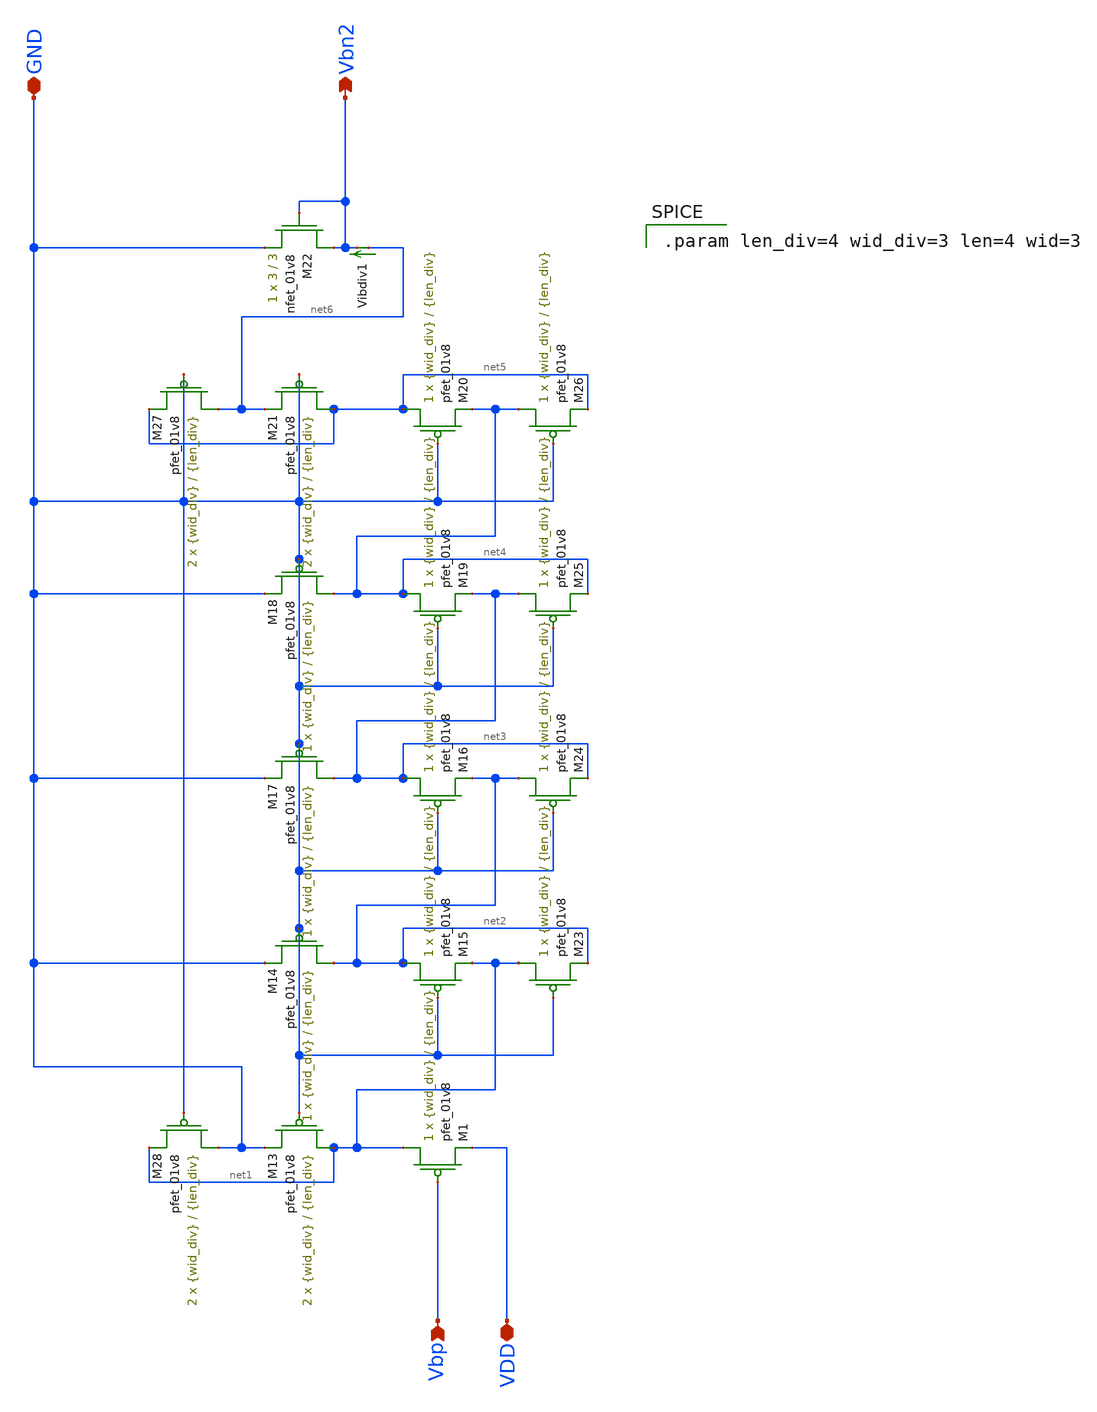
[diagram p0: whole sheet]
** sch_path: mp3/Layout_Schem_Designs/current_divider_lds.sch
**.subckt current_divider_lds GND Vbn2 Vbp VDD
*.iopin GND
*.opin Vbn2
*.ipin Vbp
*.iopin VDD
XM1 net1 Vbp VDD VDD sky130_fd_pr__pfet_01v8 L={len_div} W={wid_div} nf=1 ad='int((nf+1)/2) * W/nf * 0.29'
+ as='int((nf+2)/2) * W/nf * 0.29' pd='2*int((nf+1)/2) * (W/nf + 0.29)' ps='2*int((nf+2)/2) * (W/nf + 0.29)'
+ nrd='0.29 / W' nrs='0.29 / W' sa=0 sb=0 sd=0 mult=1 m=1
XM13 net1 GND GND VDD sky130_fd_pr__pfet_01v8 L={len_div} W={wid_div} nf=1 ad='int((nf+1)/2) * W/nf * 0.29'
+ as='int((nf+2)/2) * W/nf * 0.29' pd='2*int((nf+1)/2) * (W/nf + 0.29)' ps='2*int((nf+2)/2) * (W/nf + 0.29)'
+ nrd='0.29 / W' nrs='0.29 / W' sa=0 sb=0 sd=0 mult=2 m=2
XM14 net2 GND GND VDD sky130_fd_pr__pfet_01v8 L={len_div} W={wid_div} nf=1 ad='int((nf+1)/2) * W/nf * 0.29'
+ as='int((nf+2)/2) * W/nf * 0.29' pd='2*int((nf+1)/2) * (W/nf + 0.29)' ps='2*int((nf+2)/2) * (W/nf + 0.29)'
+ nrd='0.29 / W' nrs='0.29 / W' sa=0 sb=0 sd=0 mult=1 m=1
XM15 net2 GND net1 VDD sky130_fd_pr__pfet_01v8 L={len_div} W={wid_div} nf=1 ad='int((nf+1)/2) * W/nf * 0.29'
+ as='int((nf+2)/2) * W/nf * 0.29' pd='2*int((nf+1)/2) * (W/nf + 0.29)' ps='2*int((nf+2)/2) * (W/nf + 0.29)'
+ nrd='0.29 / W' nrs='0.29 / W' sa=0 sb=0 sd=0 mult=1 m=1
XM16 net3 GND net2 VDD sky130_fd_pr__pfet_01v8 L={len_div} W={wid_div} nf=1 ad='int((nf+1)/2) * W/nf * 0.29'
+ as='int((nf+2)/2) * W/nf * 0.29' pd='2*int((nf+1)/2) * (W/nf + 0.29)' ps='2*int((nf+2)/2) * (W/nf + 0.29)'
+ nrd='0.29 / W' nrs='0.29 / W' sa=0 sb=0 sd=0 mult=1 m=1
XM17 net3 GND GND VDD sky130_fd_pr__pfet_01v8 L={len_div} W={wid_div} nf=1 ad='int((nf+1)/2) * W/nf * 0.29'
+ as='int((nf+2)/2) * W/nf * 0.29' pd='2*int((nf+1)/2) * (W/nf + 0.29)' ps='2*int((nf+2)/2) * (W/nf + 0.29)'
+ nrd='0.29 / W' nrs='0.29 / W' sa=0 sb=0 sd=0 mult=1 m=1
XM18 net4 GND GND VDD sky130_fd_pr__pfet_01v8 L={len_div} W={wid_div} nf=1 ad='int((nf+1)/2) * W/nf * 0.29'
+ as='int((nf+2)/2) * W/nf * 0.29' pd='2*int((nf+1)/2) * (W/nf + 0.29)' ps='2*int((nf+2)/2) * (W/nf + 0.29)'
+ nrd='0.29 / W' nrs='0.29 / W' sa=0 sb=0 sd=0 mult=1 m=1
XM19 net4 GND net3 VDD sky130_fd_pr__pfet_01v8 L={len_div} W={wid_div} nf=1 ad='int((nf+1)/2) * W/nf * 0.29'
+ as='int((nf+2)/2) * W/nf * 0.29' pd='2*int((nf+1)/2) * (W/nf + 0.29)' ps='2*int((nf+2)/2) * (W/nf + 0.29)'
+ nrd='0.29 / W' nrs='0.29 / W' sa=0 sb=0 sd=0 mult=1 m=1
XM20 net5 GND net4 VDD sky130_fd_pr__pfet_01v8 L={len_div} W={wid_div} nf=1 ad='int((nf+1)/2) * W/nf * 0.29'
+ as='int((nf+2)/2) * W/nf * 0.29' pd='2*int((nf+1)/2) * (W/nf + 0.29)' ps='2*int((nf+2)/2) * (W/nf + 0.29)'
+ nrd='0.29 / W' nrs='0.29 / W' sa=0 sb=0 sd=0 mult=1 m=1
XM21 net5 GND net6 VDD sky130_fd_pr__pfet_01v8 L={len_div} W={wid_div} nf=1 ad='int((nf+1)/2) * W/nf * 0.29'
+ as='int((nf+2)/2) * W/nf * 0.29' pd='2*int((nf+1)/2) * (W/nf + 0.29)' ps='2*int((nf+2)/2) * (W/nf + 0.29)'
+ nrd='0.29 / W' nrs='0.29 / W' sa=0 sb=0 sd=0 mult=2 m=2
XM22 Vbn2 Vbn2 GND GND sky130_fd_pr__nfet_01v8 L=3 W=3 nf=1 ad='int((nf+1)/2) * W/nf * 0.29' as='int((nf+2)/2) * W/nf * 0.29'
+ pd='2*int((nf+1)/2) * (W/nf + 0.29)' ps='2*int((nf+2)/2) * (W/nf + 0.29)' nrd='0.29 / W' nrs='0.29 / W'
+ sa=0 sb=0 sd=0 mult=1 m=1
Vibdiv1 net6 Vbn2 0
.save i(vibdiv1)
XM23 net1 GND net2 VDD sky130_fd_pr__pfet_01v8 L={len_div} W={wid_div} nf=1 ad='int((nf+1)/2) * W/nf * 0.29'
+ as='int((nf+2)/2) * W/nf * 0.29' pd='2*int((nf+1)/2) * (W/nf + 0.29)' ps='2*int((nf+2)/2) * (W/nf + 0.29)'
+ nrd='0.29 / W' nrs='0.29 / W' sa=0 sb=0 sd=0 mult=1 m=1
XM24 net2 GND net3 VDD sky130_fd_pr__pfet_01v8 L={len_div} W={wid_div} nf=1 ad='int((nf+1)/2) * W/nf * 0.29'
+ as='int((nf+2)/2) * W/nf * 0.29' pd='2*int((nf+1)/2) * (W/nf + 0.29)' ps='2*int((nf+2)/2) * (W/nf + 0.29)'
+ nrd='0.29 / W' nrs='0.29 / W' sa=0 sb=0 sd=0 mult=1 m=1
XM25 net3 GND net4 VDD sky130_fd_pr__pfet_01v8 L={len_div} W={wid_div} nf=1 ad='int((nf+1)/2) * W/nf * 0.29'
+ as='int((nf+2)/2) * W/nf * 0.29' pd='2*int((nf+1)/2) * (W/nf + 0.29)' ps='2*int((nf+2)/2) * (W/nf + 0.29)'
+ nrd='0.29 / W' nrs='0.29 / W' sa=0 sb=0 sd=0 mult=1 m=1
XM26 net4 GND net5 VDD sky130_fd_pr__pfet_01v8 L={len_div} W={wid_div} nf=1 ad='int((nf+1)/2) * W/nf * 0.29'
+ as='int((nf+2)/2) * W/nf * 0.29' pd='2*int((nf+1)/2) * (W/nf + 0.29)' ps='2*int((nf+2)/2) * (W/nf + 0.29)'
+ nrd='0.29 / W' nrs='0.29 / W' sa=0 sb=0 sd=0 mult=1 m=1
XM27 net6 GND net5 VDD sky130_fd_pr__pfet_01v8 L={len_div} W={wid_div} nf=1 ad='int((nf+1)/2) * W/nf * 0.29'
+ as='int((nf+2)/2) * W/nf * 0.29' pd='2*int((nf+1)/2) * (W/nf + 0.29)' ps='2*int((nf+2)/2) * (W/nf + 0.29)'
+ nrd='0.29 / W' nrs='0.29 / W' sa=0 sb=0 sd=0 mult=2 m=2
XM28 GND GND net1 VDD sky130_fd_pr__pfet_01v8 L={len_div} W={wid_div} nf=1 ad='int((nf+1)/2) * W/nf * 0.29'
+ as='int((nf+2)/2) * W/nf * 0.29' pd='2*int((nf+1)/2) * (W/nf + 0.29)' ps='2*int((nf+2)/2) * (W/nf + 0.29)'
+ nrd='0.29 / W' nrs='0.29 / W' sa=0 sb=0 sd=0 mult=2 m=2
**** begin user architecture code

.param len_div=4 wid_div=3 len=4 wid=3

**** end user architecture code
**.ends
.end
